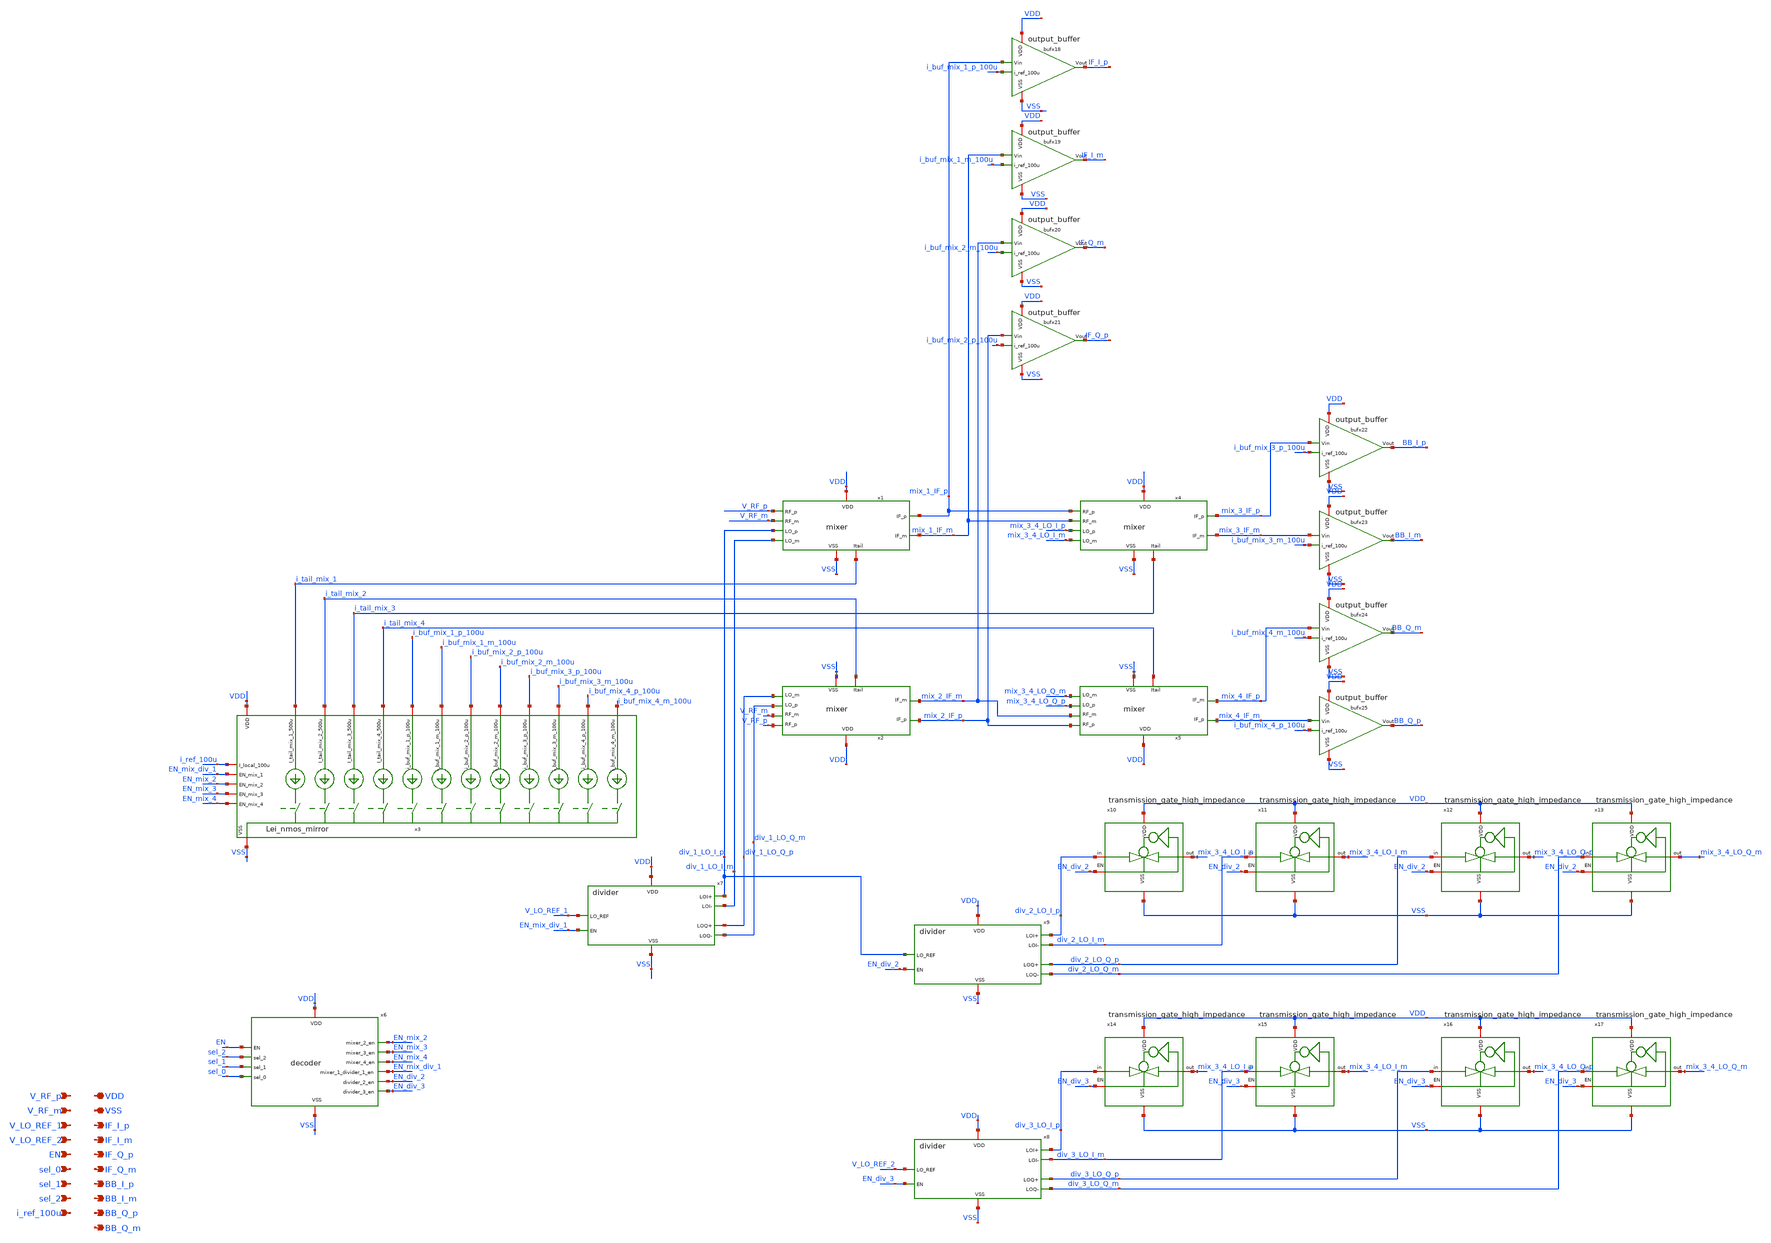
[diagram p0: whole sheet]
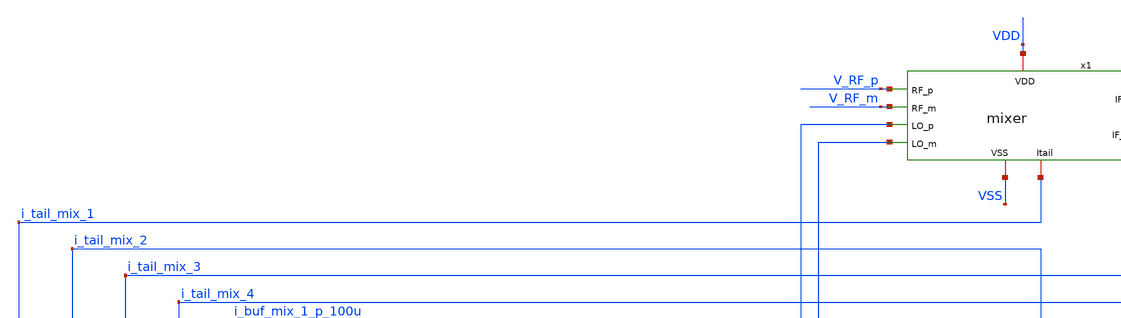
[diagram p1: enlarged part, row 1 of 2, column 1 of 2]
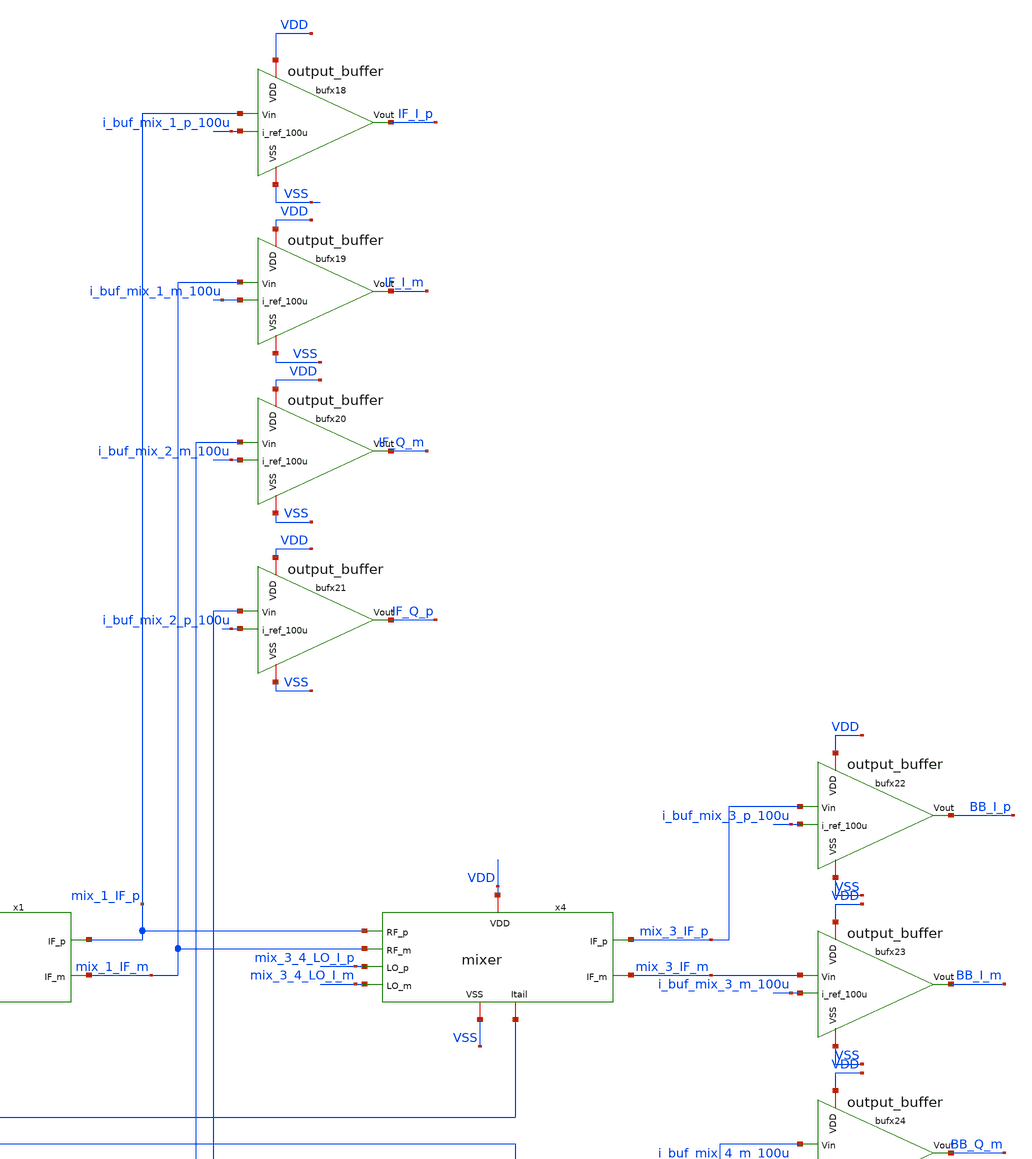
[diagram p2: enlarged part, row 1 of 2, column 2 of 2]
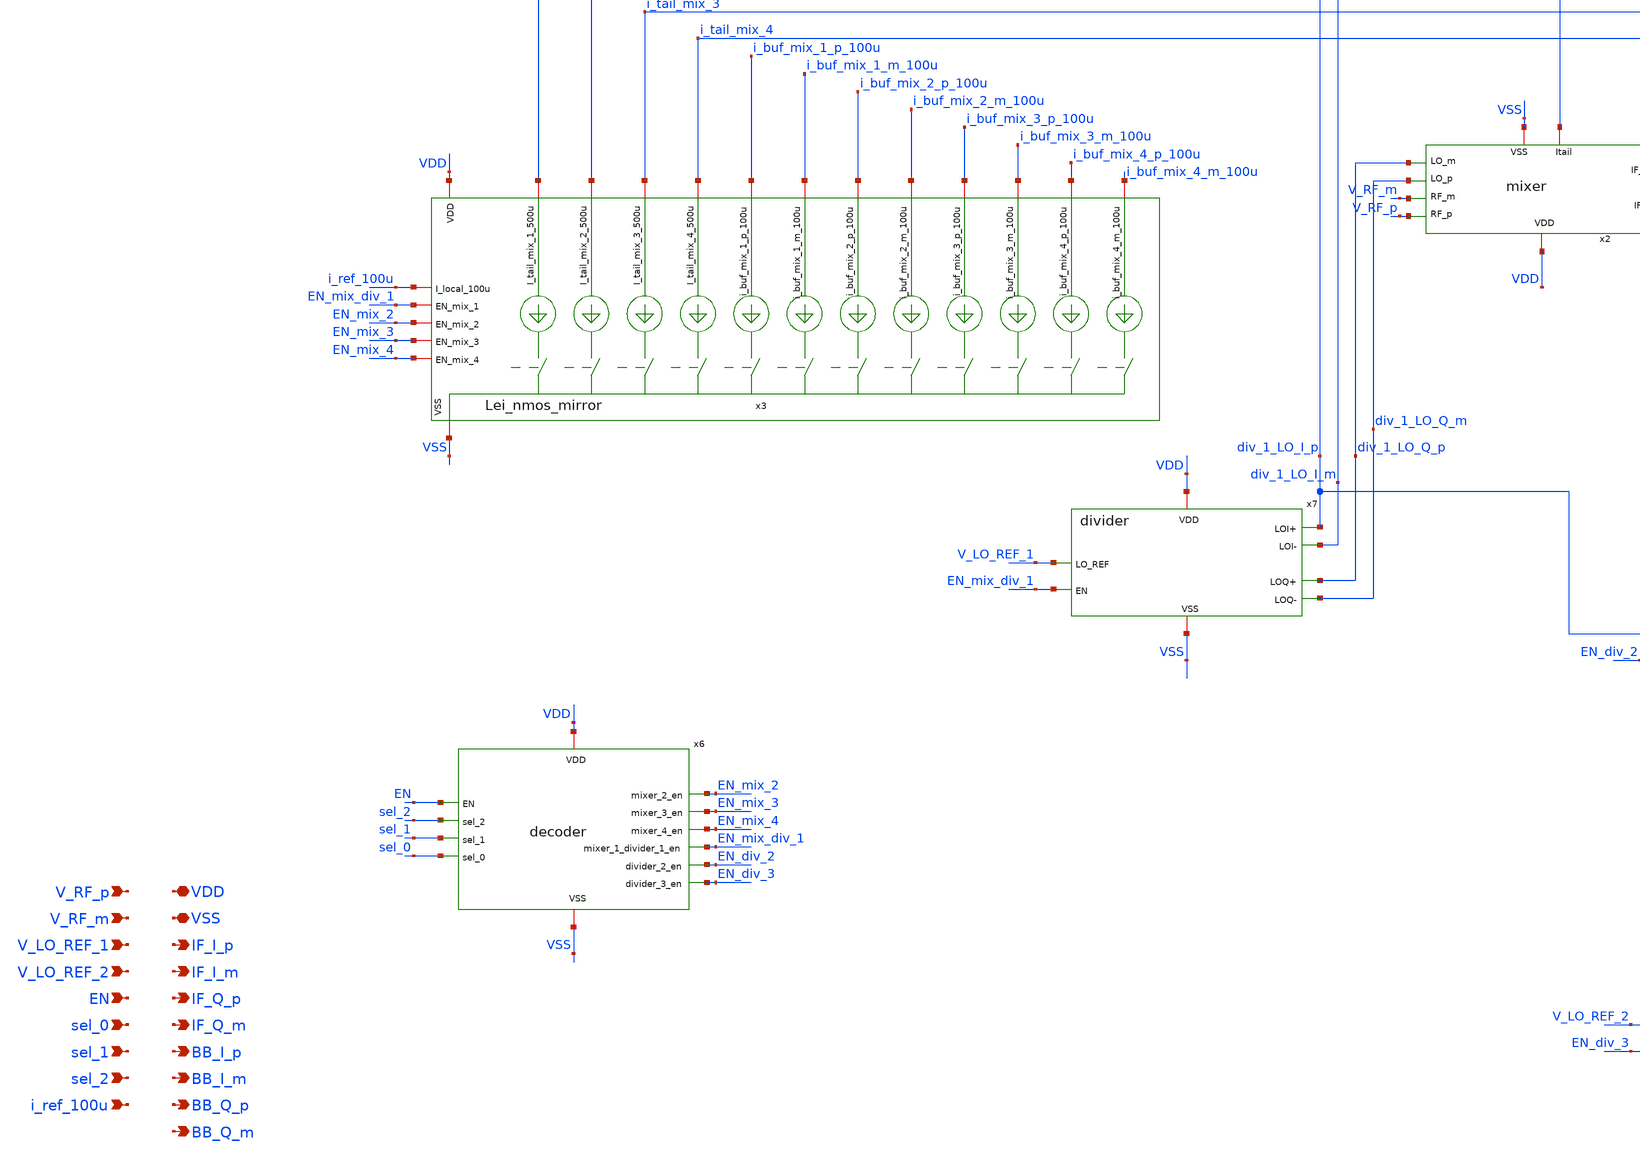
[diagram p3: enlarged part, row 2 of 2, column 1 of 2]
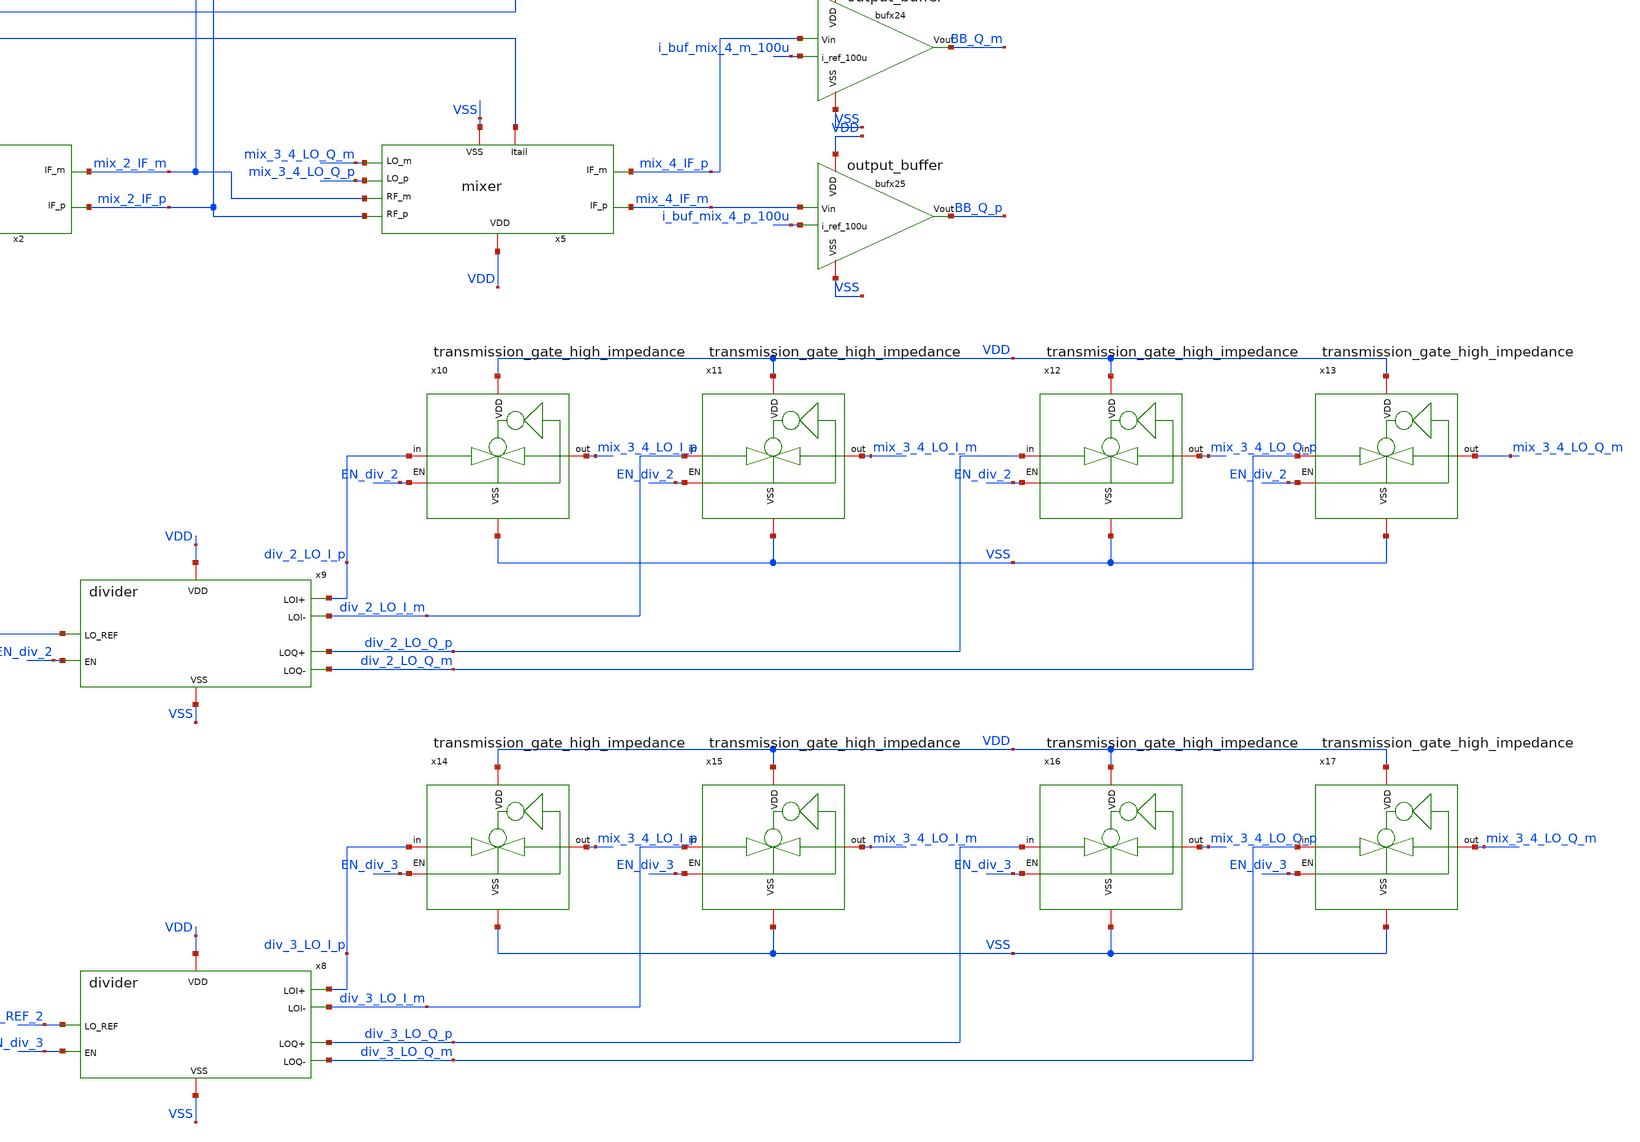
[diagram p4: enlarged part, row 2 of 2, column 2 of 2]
** sch_path: designs/top_level/schematic/top.sch
**.subckt top VDD VSS V_RF_p V_RF_m V_LO_REF_1 V_LO_REF_2 EN sel_0 sel_1 sel_2 i_ref_100u IF_I_p
*+ IF_I_m IF_Q_p IF_Q_m BB_I_p BB_I_m BB_Q_p BB_Q_m
*.iopin VDD
*.iopin VSS
*.ipin V_RF_p
*.ipin V_RF_m
*.ipin V_LO_REF_1
*.ipin V_LO_REF_2
*.ipin EN
*.ipin sel_0
*.ipin sel_1
*.ipin sel_2
*.ipin i_ref_100u
*.opin IF_I_p
*.opin IF_I_m
*.opin IF_Q_p
*.opin IF_Q_m
*.opin BB_I_p
*.opin BB_I_m
*.opin BB_Q_p
*.opin BB_Q_m
x1 mix_1_IF_p V_RF_p VDD VSS mix_1_IF_m V_RF_m div_1_LO_I_p i_tail_mix_1 div_1_LO_I_m mixer
x2 mix_2_IF_p V_RF_p VDD VSS mix_2_IF_m V_RF_m div_1_LO_Q_m i_tail_mix_2 div_1_LO_Q_p mixer
x4 mix_3_IF_p mix_1_IF_p VDD VSS mix_3_IF_m mix_1_IF_m mix_3_4_LO_I_p i_tail_mix_3 mix_3_4_LO_I_m
+ mixer
x5 mix_4_IF_m mix_2_IF_p VDD VSS mix_4_IF_p mix_2_IF_m mix_3_4_LO_Q_p i_tail_mix_4 mix_3_4_LO_Q_m
+ mixer
x6 VDD VSS EN sel_2 EN_mix_2 sel_1 EN_mix_3 EN_mix_4 sel_0 EN_div_2 EN_div_3 EN_mix_div_1 decoder
x7 VDD VSS V_LO_REF_1 div_1_LO_I_p div_1_LO_I_m div_1_LO_Q_p div_1_LO_Q_m EN_mix_div_1 divider
x8 VDD VSS V_LO_REF_2 div_3_LO_I_p div_3_LO_I_m div_3_LO_Q_p div_3_LO_Q_m EN_div_3 divider
x9 VDD VSS div_1_LO_I_p div_2_LO_I_p div_2_LO_I_m div_2_LO_Q_p div_2_LO_Q_m EN_div_2 divider
x10 VDD div_2_LO_I_p mix_3_4_LO_I_p VSS EN_div_2 transmission_gate_high_impedance
x11 VDD div_2_LO_I_m mix_3_4_LO_I_m VSS EN_div_2 transmission_gate_high_impedance
x12 VDD div_2_LO_Q_p mix_3_4_LO_Q_p VSS EN_div_2 transmission_gate_high_impedance
x13 VDD div_2_LO_Q_m mix_3_4_LO_Q_m VSS EN_div_2 transmission_gate_high_impedance
x14 VDD div_3_LO_I_p mix_3_4_LO_I_p VSS EN_div_3 transmission_gate_high_impedance
x15 VDD div_3_LO_I_m mix_3_4_LO_I_m VSS EN_div_3 transmission_gate_high_impedance
x16 VDD div_3_LO_Q_p mix_3_4_LO_Q_p VSS EN_div_3 transmission_gate_high_impedance
x17 VDD div_3_LO_Q_m mix_3_4_LO_Q_m VSS EN_div_3 transmission_gate_high_impedance
x18 IF_I_p mix_1_IF_p i_buf_mix_1_p_100u VDD VSS output_buffer
x19 IF_I_m mix_1_IF_m i_buf_mix_1_m_100u VDD VSS output_buffer
x20 IF_Q_m mix_2_IF_m i_buf_mix_2_m_100u VDD VSS output_buffer
x21 IF_Q_p mix_2_IF_p i_buf_mix_2_p_100u VDD VSS output_buffer
x22 BB_I_p mix_3_IF_p i_buf_mix_3_p_100u VDD VSS output_buffer
x23 BB_I_m mix_3_IF_m i_buf_mix_3_m_100u VDD VSS output_buffer
x24 BB_Q_m mix_4_IF_p i_buf_mix_4_m_100u VDD VSS output_buffer
x25 BB_Q_p mix_4_IF_m i_buf_mix_4_p_100u VDD VSS output_buffer
x3 VDD i_tail_mix_1 EN_mix_div_1 EN_mix_2 EN_mix_3 EN_mix_4 i_tail_mix_2 i_tail_mix_3 i_ref_100u
+ i_tail_mix_4 VSS i_buf_mix_1_p_100u i_buf_mix_1_m_100u i_buf_mix_2_p_100u i_buf_mix_2_m_100u i_buf_mix_3_p_100u
+ i_buf_mix_3_m_100u i_buf_mix_4_p_100u i_buf_mix_4_m_100u Lei_nmos_mirror
**.ends
.end
